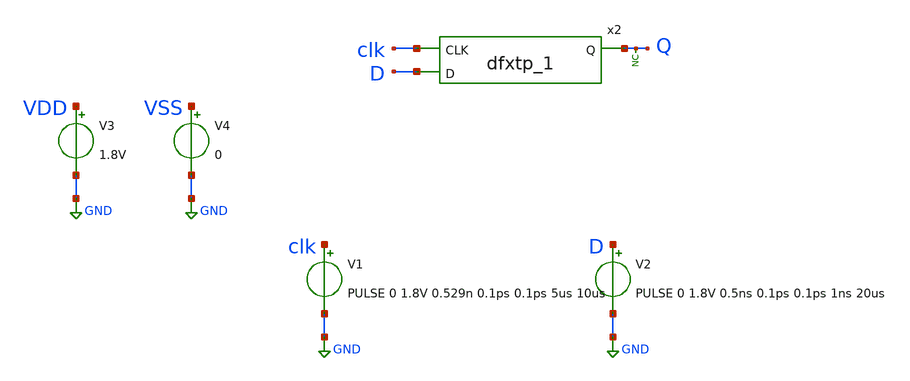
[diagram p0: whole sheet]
** sch_path: xschem/tests/dummy_tests/dff_timing.sch
**.subckt dff_timing
V3 VDD GND 1.8V
V4 VSS GND 0
V1 clk GND PULSE 0 1.8V 0.529n 0.1ps 0.1ps 5us 10us
V2 D GND PULSE 0 1.8V 0.5ns 0.1ps 0.1ps 1ns 20us
x2 clk D VSS VSS VDD VDD Q sky130_fd_sc_hd__dfxtp_1
* noconn Q
**** begin user architecture code
 .lib $::SKYWATER_MODELS/sky130.lib.spice tt
.include $::SKYWATER_STDCELLS/sky130_fd_sc_hd.spice


.options acct list
.temp 25
*vvcc VDD 0 dc 1.8
*vvss VSS 0 0
.control
tran 0.001n 1.5n
*plot RST_PLS clk+2 Pulse+4
plot clk D+2 Q+4
write dff_timing.raw
.endc


**** end user architecture code
**.ends
.GLOBAL GND
.end
